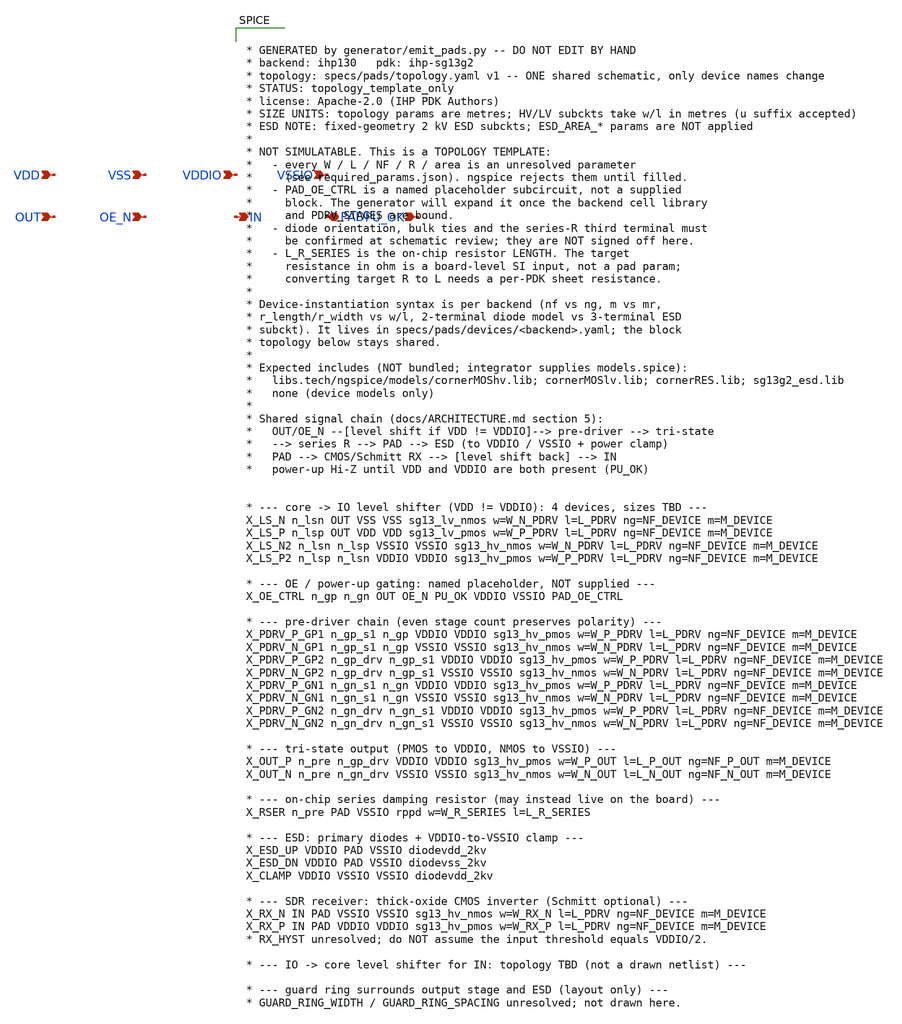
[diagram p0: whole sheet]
** sch_path: sch/pads/ihp130/sdr_bidir_pad.sch
**.subckt sdr_bidir_pad OUT OE_N IN PAD PU_OK VDD VSS VDDIO VSSIO
*.ipin OUT
*.ipin OE_N
*.opin IN
*.iopin PAD
*.ipin PU_OK
*.ipin VDD
*.ipin VSS
*.ipin VDDIO
*.ipin VSSIO
**** begin user architecture code


* GENERATED by generator/emit_pads.py -- DO NOT EDIT BY HAND
* backend: ihp130   pdk: ihp-sg13g2
* topology: specs/pads/topology.yaml v1 -- ONE shared schematic, only device names change
* STATUS: topology_template_only
* license: Apache-2.0 (IHP PDK Authors)
* SIZE UNITS: topology params are metres; HV/LV subckts take w/l in metres (u suffix accepted)
* ESD NOTE: fixed-geometry 2 kV ESD subckts; ESD_AREA_* params are NOT applied
*
* NOT SIMULATABLE. This is a TOPOLOGY TEMPLATE:
*   - every W / L / NF / R / area is an unresolved parameter
*     (see required_params.json). ngspice rejects them until filled.
*   - PAD_OE_CTRL is a named placeholder subcircuit, not a supplied
*     block. The generator will expand it once the backend cell library
*     and PDRV_STAGES are bound.
*   - diode orientation, bulk ties and the series-R third terminal must
*     be confirmed at schematic review; they are NOT signed off here.
*   - L_R_SERIES is the on-chip resistor LENGTH. The target
*     resistance in ohm is a board-level SI input, not a pad param;
*     converting target R to L needs a per-PDK sheet resistance.
*
* Device-instantiation syntax is per backend (nf vs ng, m vs mr,
* r_length/r_width vs w/l, 2-terminal diode model vs 3-terminal ESD
* subckt). It lives in specs/pads/devices/<backend>.yaml; the block
* topology below stays shared.
*
* Expected includes (NOT bundled; integrator supplies models.spice):
*   libs.tech/ngspice/models/cornerMOShv.lib; cornerMOSlv.lib; cornerRES.lib; sg13g2_esd.lib
*   none (device models only)
*
* Shared signal chain (docs/ARCHITECTURE.md section 5):
*   OUT/OE_N --[level shift if VDD != VDDIO]--> pre-driver --> tri-state
*   --> series R --> PAD --> ESD (to VDDIO / VSSIO + power clamp)
*   PAD --> CMOS/Schmitt RX --> [level shift back] --> IN
*   power-up Hi-Z until VDD and VDDIO are both present (PU_OK)


* --- core -> IO level shifter (VDD != VDDIO): 4 devices, sizes TBD ---
X_LS_N n_lsn OUT VSS VSS sg13_lv_nmos w=W_N_PDRV l=L_PDRV ng=NF_DEVICE m=M_DEVICE
X_LS_P n_lsp OUT VDD VDD sg13_lv_pmos w=W_P_PDRV l=L_PDRV ng=NF_DEVICE m=M_DEVICE
X_LS_N2 n_lsn n_lsp VSSIO VSSIO sg13_hv_nmos w=W_N_PDRV l=L_PDRV ng=NF_DEVICE m=M_DEVICE
X_LS_P2 n_lsp n_lsn VDDIO VDDIO sg13_hv_pmos w=W_P_PDRV l=L_PDRV ng=NF_DEVICE m=M_DEVICE

* --- OE / power-up gating: named placeholder, NOT supplied ---
X_OE_CTRL n_gp n_gn OUT OE_N PU_OK VDDIO VSSIO PAD_OE_CTRL

* --- pre-driver chain (even stage count preserves polarity) ---
X_PDRV_P_GP1 n_gp_s1 n_gp VDDIO VDDIO sg13_hv_pmos w=W_P_PDRV l=L_PDRV ng=NF_DEVICE m=M_DEVICE
X_PDRV_N_GP1 n_gp_s1 n_gp VSSIO VSSIO sg13_hv_nmos w=W_N_PDRV l=L_PDRV ng=NF_DEVICE m=M_DEVICE
X_PDRV_P_GP2 n_gp_drv n_gp_s1 VDDIO VDDIO sg13_hv_pmos w=W_P_PDRV l=L_PDRV ng=NF_DEVICE m=M_DEVICE
X_PDRV_N_GP2 n_gp_drv n_gp_s1 VSSIO VSSIO sg13_hv_nmos w=W_N_PDRV l=L_PDRV ng=NF_DEVICE m=M_DEVICE
X_PDRV_P_GN1 n_gn_s1 n_gn VDDIO VDDIO sg13_hv_pmos w=W_P_PDRV l=L_PDRV ng=NF_DEVICE m=M_DEVICE
X_PDRV_N_GN1 n_gn_s1 n_gn VSSIO VSSIO sg13_hv_nmos w=W_N_PDRV l=L_PDRV ng=NF_DEVICE m=M_DEVICE
X_PDRV_P_GN2 n_gn_drv n_gn_s1 VDDIO VDDIO sg13_hv_pmos w=W_P_PDRV l=L_PDRV ng=NF_DEVICE m=M_DEVICE
X_PDRV_N_GN2 n_gn_drv n_gn_s1 VSSIO VSSIO sg13_hv_nmos w=W_N_PDRV l=L_PDRV ng=NF_DEVICE m=M_DEVICE

* --- tri-state output (PMOS to VDDIO, NMOS to VSSIO) ---
X_OUT_P n_pre n_gp_drv VDDIO VDDIO sg13_hv_pmos w=W_P_OUT l=L_P_OUT ng=NF_P_OUT m=M_DEVICE
X_OUT_N n_pre n_gn_drv VSSIO VSSIO sg13_hv_nmos w=W_N_OUT l=L_N_OUT ng=NF_N_OUT m=M_DEVICE

* --- on-chip series damping resistor (may instead live on the board) ---
X_RSER n_pre PAD VSSIO rppd w=W_R_SERIES l=L_R_SERIES

* --- ESD: primary diodes + VDDIO-to-VSSIO clamp ---
X_ESD_UP VDDIO PAD VSSIO diodevdd_2kv
X_ESD_DN VDDIO PAD VSSIO diodevss_2kv
X_CLAMP VDDIO VSSIO VSSIO diodevdd_2kv

* --- SDR receiver: thick-oxide CMOS inverter (Schmitt optional) ---
X_RX_N IN PAD VSSIO VSSIO sg13_hv_nmos w=W_RX_N l=L_PDRV ng=NF_DEVICE m=M_DEVICE
X_RX_P IN PAD VDDIO VDDIO sg13_hv_pmos w=W_RX_P l=L_PDRV ng=NF_DEVICE m=M_DEVICE
* RX_HYST unresolved; do NOT assume the input threshold equals VDDIO/2.

* --- IO -> core level shifter for IN: topology TBD (not a drawn netlist) ---

* --- guard ring surrounds output stage and ESD (layout only) ---
* GUARD_RING_WIDTH / GUARD_RING_SPACING unresolved; not drawn here.


**** end user architecture code
**.ends
.end
